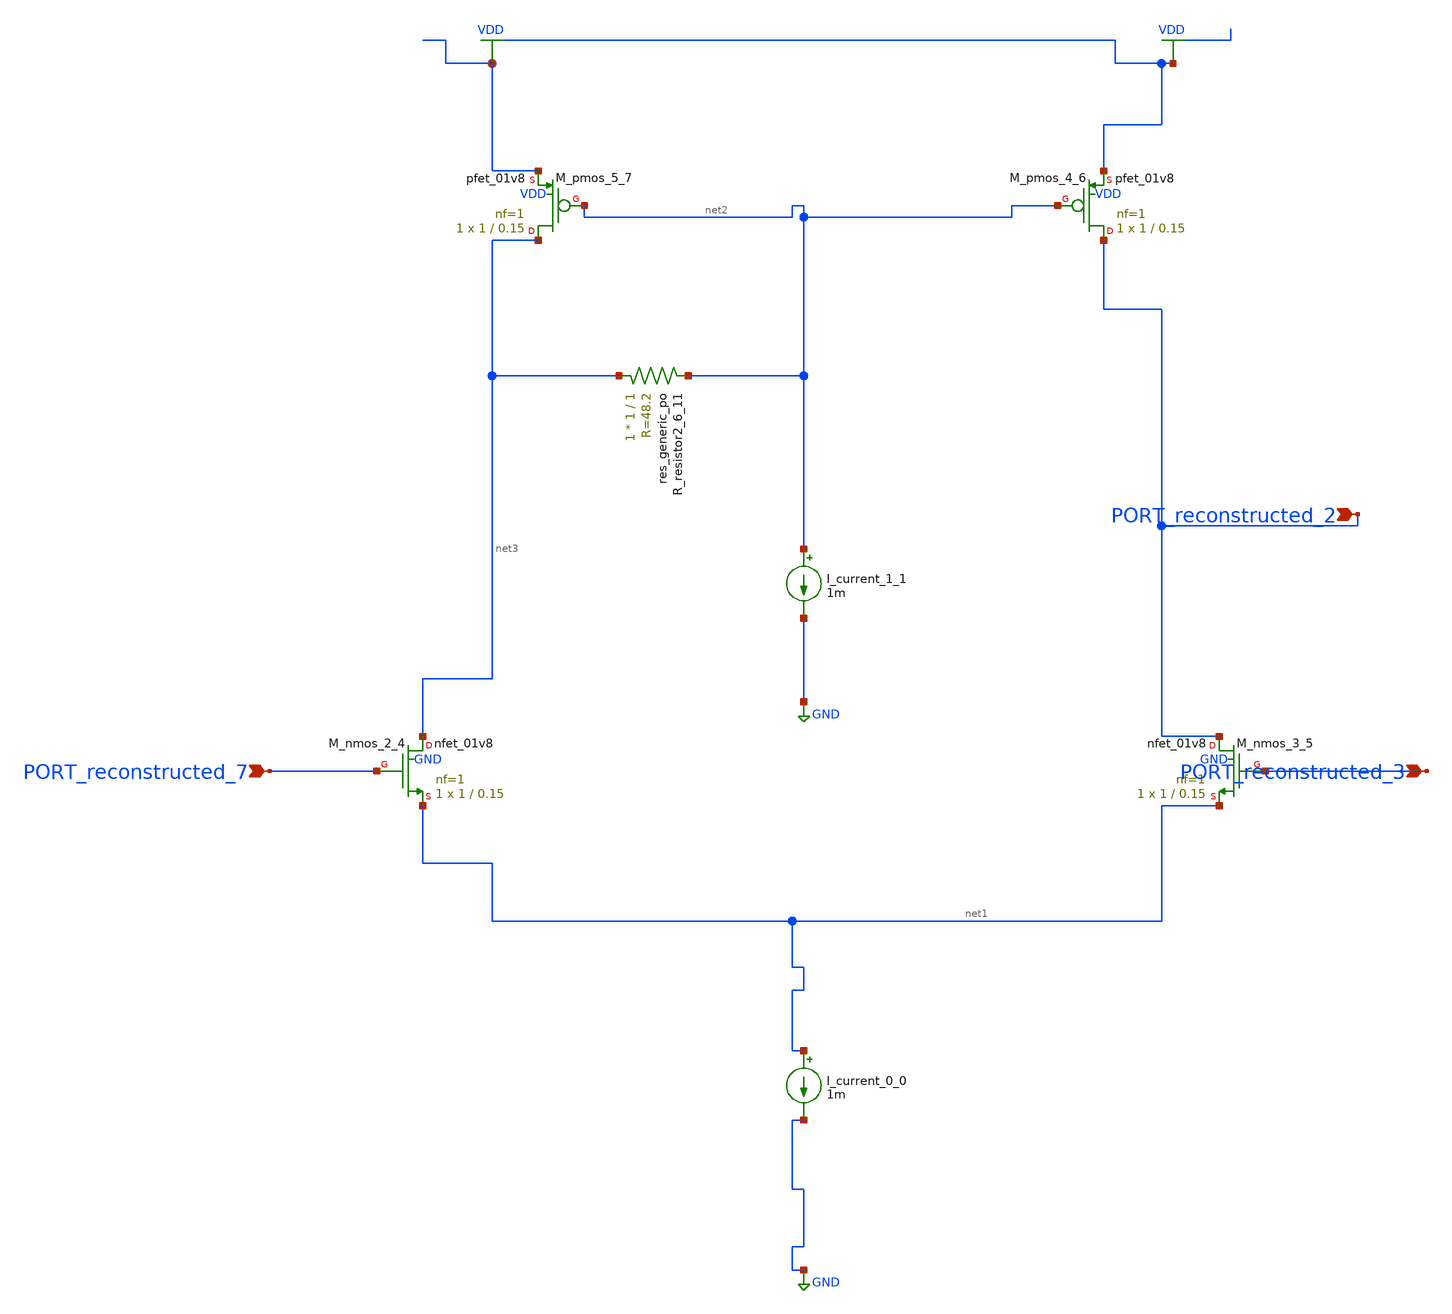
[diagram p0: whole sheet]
** sch_path: schematics/AMSNet/286.sch
**.subckt 286 PORT_reconstructed_7 PORT_reconstructed_3 PORT_reconstructed_2
*.ipin PORT_reconstructed_7
*.ipin PORT_reconstructed_3
*.ipin PORT_reconstructed_2
I_current_0_0 net1 GND 1m
I_current_1_1 net2 GND 1m
XM_nmos_2_4 net3 PORT_reconstructed_7 net1 GND sky130_fd_pr__nfet_01v8 L=0.15 W=1 nf=1 ad='int((1 + 1)/2) * 1 / 1 * 0.29'
+ as='int((1 + 2)/2) * 1 / 1 * 0.29' pd='2*int((1 + 1)/2) * (1 / 1 + 0.29)' ps='2*int((1 + 2)/2) * (1 / 1 + 0.29)'
+ nrd='0.29 / 1 ' nrs='0.29 / 1 ' sa=0 sb=0 sd=0 mult=1 m=1
XM_nmos_3_5 PORT_reconstructed_2 PORT_reconstructed_3 net1 GND sky130_fd_pr__nfet_01v8 L=0.15 W=1 nf=1
+ ad='int((1 + 1)/2) * 1 / 1 * 0.29' as='int((1 + 2)/2) * 1 / 1 * 0.29' pd='2*int((1 + 1)/2) * (1 / 1 + 0.29)'
+ ps='2*int((1 + 2)/2) * (1 / 1 + 0.29)' nrd='0.29 / 1 ' nrs='0.29 / 1 ' sa=0 sb=0 sd=0 mult=1 m=1
XM_pmos_4_6 PORT_reconstructed_2 net2 VDD VDD sky130_fd_pr__pfet_01v8 L=0.15 W=1 nf=1 ad='int((1 + 1)/2) * 1 / 1 * 0.29'
+ as='int((1 + 2)/2) * 1 / 1 * 0.29' pd='2*int((1 + 1)/2) * (1 / 1 + 0.29)' ps='2*int((1 + 2)/2) * (1 / 1 + 0.29)'
+ nrd='0.29 / 1 ' nrs='0.29 / 1 ' sa=0 sb=0 sd=0 mult=1 m=1
XM_pmos_5_7 net3 net2 VDD VDD sky130_fd_pr__pfet_01v8 L=0.15 W=1 nf=1 ad='int((1 + 1)/2) * 1 / 1 * 0.29'
+ as='int((1 + 2)/2) * 1 / 1 * 0.29' pd='2*int((1 + 1)/2) * (1 / 1 + 0.29)' ps='2*int((1 + 2)/2) * (1 / 1 + 0.29)'
+ nrd='0.29 / 1 ' nrs='0.29 / 1 ' sa=0 sb=0 sd=0 mult=1 m=1
XR_resistor2_6_11 net3 net2 sky130_fd_pr__res_generic_po W=1 L=1 m=1
**.ends
.GLOBAL GND
.GLOBAL VDD
.end
